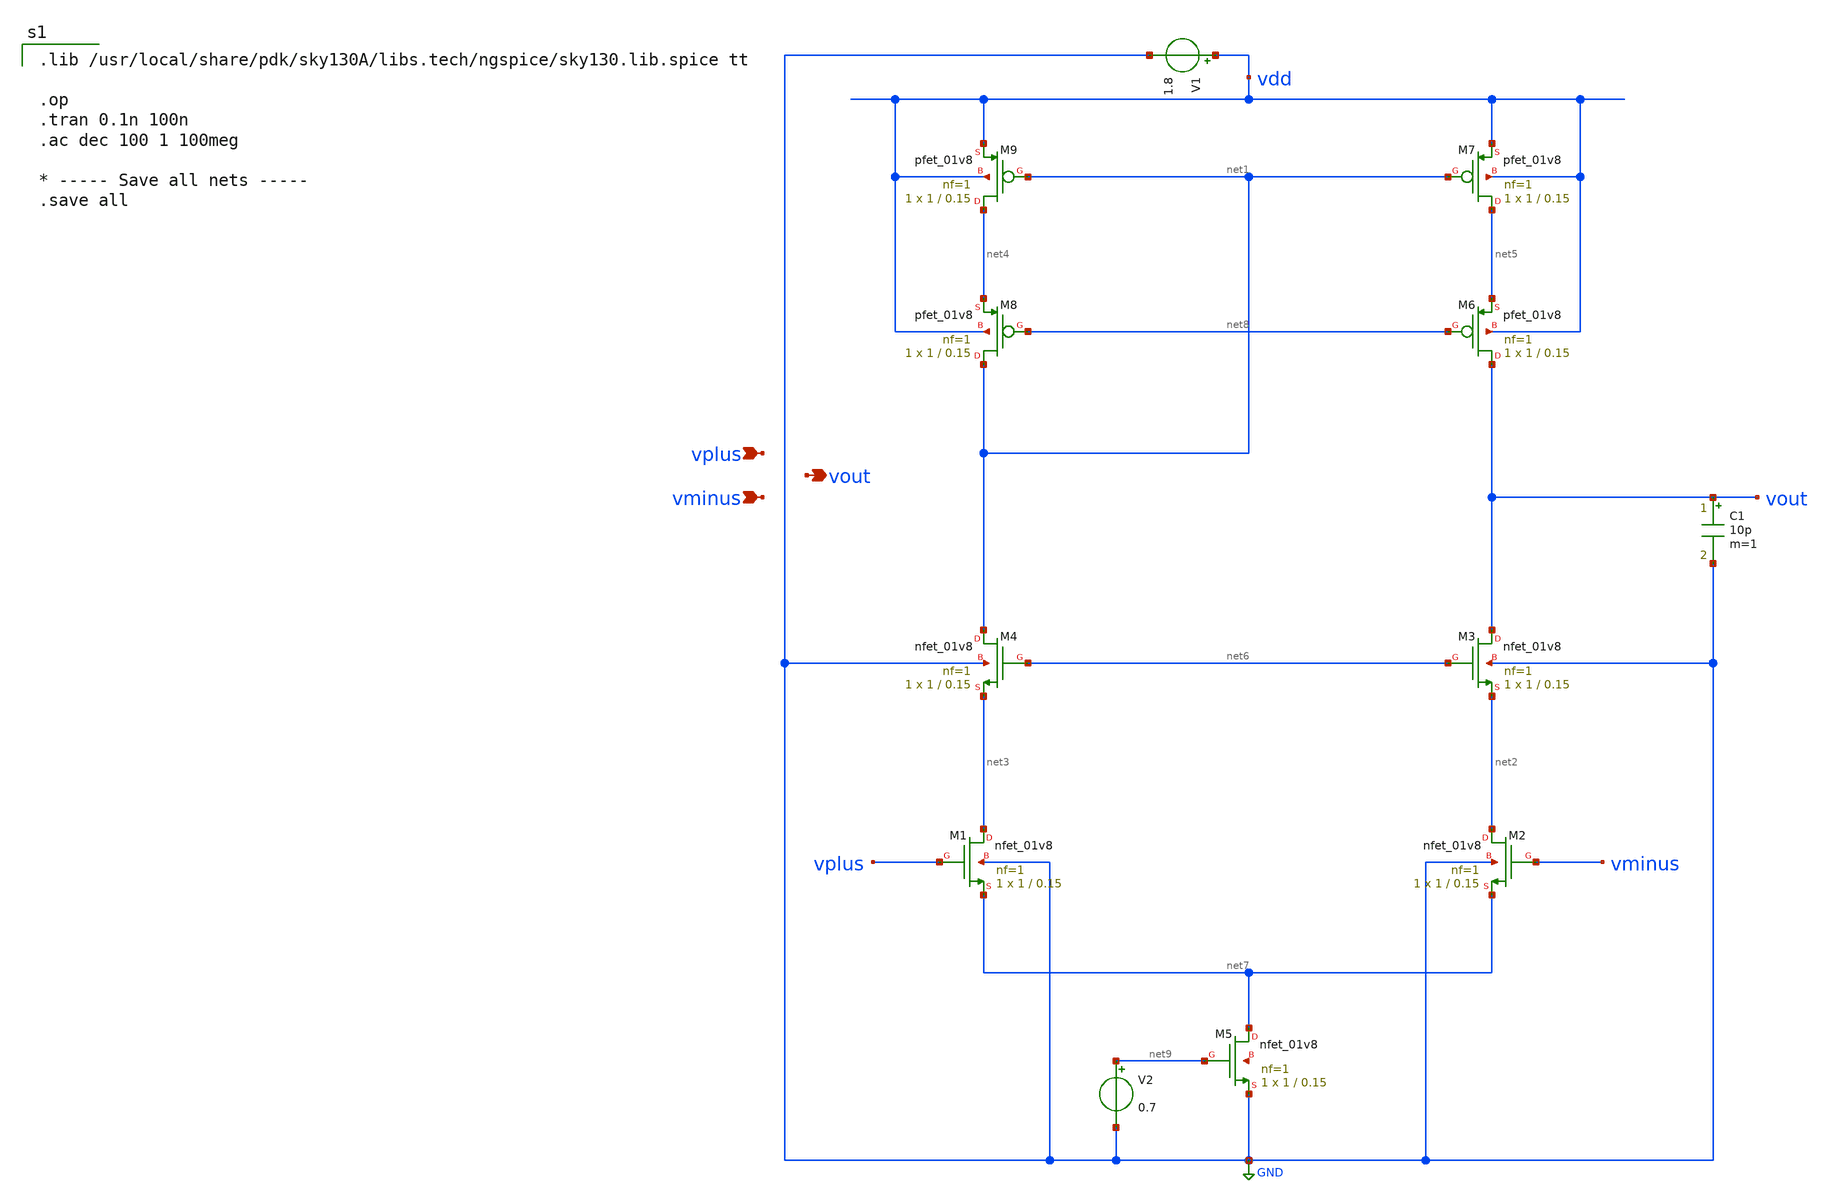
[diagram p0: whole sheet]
** sch_path: 9T_OTA_telescopic.sch
**.subckt 9T_OTA_telescopic vplus vminus vout
*.ipin vplus
*.ipin vminus
*.opin vout
XM1 net3 vplus net7 GND sky130_fd_pr__nfet_01v8 L=0.15 W=1 nf=1 ad='int((1 + 1)/2) * 1 / 1 * 0.29' as='int((1 + 2)/2) * 1 / 1 * 0.29'
+ pd='2*int((1 + 1)/2) * (1 / 1 + 0.29)' ps='2*int((1 + 2)/2) * (1 / 1 + 0.29)' nrd='0.29 / 1 ' nrs='0.29 / 1 '
+ sa=0 sb=0 sd=0 mult=1 m=1
XM2 net2 vminus net7 GND sky130_fd_pr__nfet_01v8 L=0.15 W=1 nf=1 ad='int((1 + 1)/2) * 1 / 1 * 0.29' as='int((1 + 2)/2) * 1 / 1 * 0.29'
+ pd='2*int((1 + 1)/2) * (1 / 1 + 0.29)' ps='2*int((1 + 2)/2) * (1 / 1 + 0.29)' nrd='0.29 / 1 ' nrs='0.29 / 1 '
+ sa=0 sb=0 sd=0 mult=1 m=1
XM3 vout net6 net2 GND sky130_fd_pr__nfet_01v8 L=0.15 W=1 nf=1 ad='int((1 + 1)/2) * 1 / 1 * 0.29' as='int((1 + 2)/2) * 1 / 1 * 0.29'
+ pd='2*int((1 + 1)/2) * (1 / 1 + 0.29)' ps='2*int((1 + 2)/2) * (1 / 1 + 0.29)' nrd='0.29 / 1 ' nrs='0.29 / 1 '
+ sa=0 sb=0 sd=0 mult=1 m=1
XM4 net1 net6 net3 GND sky130_fd_pr__nfet_01v8 L=0.15 W=1 nf=1 ad='int((1 + 1)/2) * 1 / 1 * 0.29' as='int((1 + 2)/2) * 1 / 1 * 0.29'
+ pd='2*int((1 + 1)/2) * (1 / 1 + 0.29)' ps='2*int((1 + 2)/2) * (1 / 1 + 0.29)' nrd='0.29 / 1 ' nrs='0.29 / 1 '
+ sa=0 sb=0 sd=0 mult=1 m=1
XM5 net7 net9 GND net10 sky130_fd_pr__nfet_01v8 L=0.15 W=1 nf=1 ad='int((1 + 1)/2) * 1 / 1 * 0.29' as='int((1 + 2)/2) * 1 / 1 * 0.29'
+ pd='2*int((1 + 1)/2) * (1 / 1 + 0.29)' ps='2*int((1 + 2)/2) * (1 / 1 + 0.29)' nrd='0.29 / 1 ' nrs='0.29 / 1 '
+ sa=0 sb=0 sd=0 mult=1 m=1
XM6 vout net8 net5 vdd sky130_fd_pr__pfet_01v8 L=0.15 W=1 nf=1 ad='int((1 + 1)/2) * 1 / 1 * 0.29' as='int((1 + 2)/2) * 1 / 1 * 0.29'
+ pd='2*int((1 + 1)/2) * (1 / 1 + 0.29)' ps='2*int((1 + 2)/2) * (1 / 1 + 0.29)' nrd='0.29 / 1 ' nrs='0.29 / 1 '
+ sa=0 sb=0 sd=0 mult=1 m=1
XM7 net5 net1 vdd vdd sky130_fd_pr__pfet_01v8 L=0.15 W=1 nf=1 ad='int((1 + 1)/2) * 1 / 1 * 0.29' as='int((1 + 2)/2) * 1 / 1 * 0.29'
+ pd='2*int((1 + 1)/2) * (1 / 1 + 0.29)' ps='2*int((1 + 2)/2) * (1 / 1 + 0.29)' nrd='0.29 / 1 ' nrs='0.29 / 1 '
+ sa=0 sb=0 sd=0 mult=1 m=1
XM8 net1 net8 net4 vdd sky130_fd_pr__pfet_01v8 L=0.15 W=1 nf=1 ad='int((1 + 1)/2) * 1 / 1 * 0.29' as='int((1 + 2)/2) * 1 / 1 * 0.29'
+ pd='2*int((1 + 1)/2) * (1 / 1 + 0.29)' ps='2*int((1 + 2)/2) * (1 / 1 + 0.29)' nrd='0.29 / 1 ' nrs='0.29 / 1 '
+ sa=0 sb=0 sd=0 mult=1 m=1
XM9 net4 net1 vdd vdd sky130_fd_pr__pfet_01v8 L=0.15 W=1 nf=1 ad='int((1 + 1)/2) * 1 / 1 * 0.29' as='int((1 + 2)/2) * 1 / 1 * 0.29'
+ pd='2*int((1 + 1)/2) * (1 / 1 + 0.29)' ps='2*int((1 + 2)/2) * (1 / 1 + 0.29)' nrd='0.29 / 1 ' nrs='0.29 / 1 '
+ sa=0 sb=0 sd=0 mult=1 m=1
C1 vout GND 10p m=1
V1 vdd GND 1.8
V2 net9 GND 0.7
**** begin user architecture code

.lib /usr/local/share/pdk/sky130A/libs.tech/ngspice/sky130.lib.spice tt

.op
.tran 0.1n 100n
.ac dec 100 1 100meg

* ----- Save all nets -----
.save all

**** end user architecture code
**.ends
.GLOBAL GND
.end
